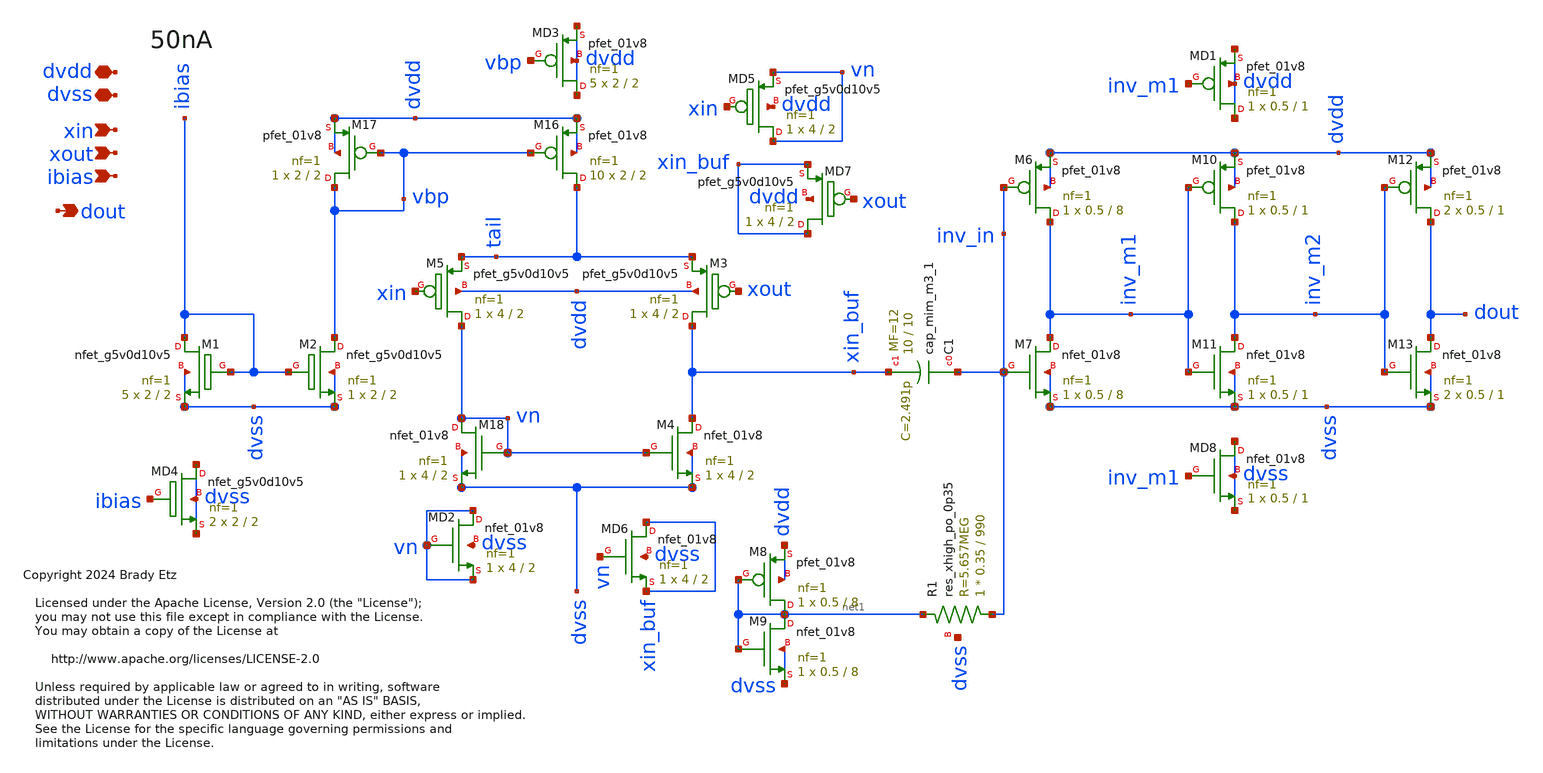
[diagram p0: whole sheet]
** sch_path: xschem/dout_amp.sch
* Copyright 2024 Brady Etz
* Licensed under the Apache License, Version 2.0 (the "License");
**.subckt dout_amp xin dvdd dvss dout ibias xout
*.ipin xin
*.iopin dvdd
*.iopin dvss
*.opin dout
*.ipin ibias
*.ipin xout
XM1 ibias ibias dvss dvss sky130_fd_pr__nfet_g5v0d10v5 L=2 W=2 nf=1 ad='int((nf+1)/2) * W/nf * 0.29'
+ as='int((nf+2)/2) * W/nf * 0.29' pd='2*int((nf+1)/2) * (W/nf + 0.29)' ps='2*int((nf+2)/2) * (W/nf + 0.29)'
+ nrd='0.29 / W' nrs='0.29 / W' sa=0 sb=0 sd=0 mult=5 m=5
XM2 vbp ibias dvss dvss sky130_fd_pr__nfet_g5v0d10v5 L=2 W=2 nf=1 ad='int((nf+1)/2) * W/nf * 0.29' as='int((nf+2)/2) * W/nf * 0.29'
+ pd='2*int((nf+1)/2) * (W/nf + 0.29)' ps='2*int((nf+2)/2) * (W/nf + 0.29)' nrd='0.29 / W' nrs='0.29 / W'
+ sa=0 sb=0 sd=0 mult=1 m=1
XM5 vn xin tail dvdd sky130_fd_pr__pfet_g5v0d10v5 L=2 W=4 nf=1 ad='int((nf+1)/2) * W/nf * 0.29' as='int((nf+2)/2) * W/nf * 0.29'
+ pd='2*int((nf+1)/2) * (W/nf + 0.29)' ps='2*int((nf+2)/2) * (W/nf + 0.29)' nrd='0.29 / W' nrs='0.29 / W'
+ sa=0 sb=0 sd=0 mult=1 m=1
XC1 inv_in xin_buf sky130_fd_pr__cap_mim_m3_1 W=10 L=10 MF=12 m=12
XM6 inv_m1 inv_in dvdd dvdd sky130_fd_pr__pfet_01v8 L=8 W=0.5 nf=1 ad='int((nf+1)/2) * W/nf * 0.29' as='int((nf+2)/2) * W/nf * 0.29'
+ pd='2*int((nf+1)/2) * (W/nf + 0.29)' ps='2*int((nf+2)/2) * (W/nf + 0.29)' nrd='0.29 / W' nrs='0.29 / W'
+ sa=0 sb=0 sd=0 mult=1 m=1
XM7 inv_m1 inv_in dvss dvss sky130_fd_pr__nfet_01v8 L=8 W=0.5 nf=1 ad='int((nf+1)/2) * W/nf * 0.29' as='int((nf+2)/2) * W/nf * 0.29'
+ pd='2*int((nf+1)/2) * (W/nf + 0.29)' ps='2*int((nf+2)/2) * (W/nf + 0.29)' nrd='0.29 / W' nrs='0.29 / W'
+ sa=0 sb=0 sd=0 mult=1 m=1
XM8 net1 net1 dvdd dvdd sky130_fd_pr__pfet_01v8 L=8 W=0.5 nf=1 ad='int((nf+1)/2) * W/nf * 0.29' as='int((nf+2)/2) * W/nf * 0.29'
+ pd='2*int((nf+1)/2) * (W/nf + 0.29)' ps='2*int((nf+2)/2) * (W/nf + 0.29)' nrd='0.29 / W' nrs='0.29 / W'
+ sa=0 sb=0 sd=0 mult=1 m=1
XM9 net1 net1 dvss dvss sky130_fd_pr__nfet_01v8 L=8 W=0.5 nf=1 ad='int((nf+1)/2) * W/nf * 0.29' as='int((nf+2)/2) * W/nf * 0.29'
+ pd='2*int((nf+1)/2) * (W/nf + 0.29)' ps='2*int((nf+2)/2) * (W/nf + 0.29)' nrd='0.29 / W' nrs='0.29 / W'
+ sa=0 sb=0 sd=0 mult=1 m=1
XR1 inv_in net1 dvss sky130_fd_pr__res_xhigh_po_0p35 L=990 mult=1 m=1
XM10 inv_m2 inv_m1 dvdd dvdd sky130_fd_pr__pfet_01v8 L=1 W=0.5 nf=1 ad='int((nf+1)/2) * W/nf * 0.29'
+ as='int((nf+2)/2) * W/nf * 0.29' pd='2*int((nf+1)/2) * (W/nf + 0.29)' ps='2*int((nf+2)/2) * (W/nf + 0.29)'
+ nrd='0.29 / W' nrs='0.29 / W' sa=0 sb=0 sd=0 mult=1 m=1
XM11 inv_m2 inv_m1 dvss dvss sky130_fd_pr__nfet_01v8 L=1 W=0.5 nf=1 ad='int((nf+1)/2) * W/nf * 0.29'
+ as='int((nf+2)/2) * W/nf * 0.29' pd='2*int((nf+1)/2) * (W/nf + 0.29)' ps='2*int((nf+2)/2) * (W/nf + 0.29)'
+ nrd='0.29 / W' nrs='0.29 / W' sa=0 sb=0 sd=0 mult=1 m=1
XM12 dout inv_m2 dvdd dvdd sky130_fd_pr__pfet_01v8 L=1 W=0.5 nf=1 ad='int((nf+1)/2) * W/nf * 0.29' as='int((nf+2)/2) * W/nf * 0.29'
+ pd='2*int((nf+1)/2) * (W/nf + 0.29)' ps='2*int((nf+2)/2) * (W/nf + 0.29)' nrd='0.29 / W' nrs='0.29 / W'
+ sa=0 sb=0 sd=0 mult=2 m=2
XM13 dout inv_m2 dvss dvss sky130_fd_pr__nfet_01v8 L=1 W=0.5 nf=1 ad='int((nf+1)/2) * W/nf * 0.29' as='int((nf+2)/2) * W/nf * 0.29'
+ pd='2*int((nf+1)/2) * (W/nf + 0.29)' ps='2*int((nf+2)/2) * (W/nf + 0.29)' nrd='0.29 / W' nrs='0.29 / W'
+ sa=0 sb=0 sd=0 mult=2 m=2
XM16 tail vbp dvdd dvdd sky130_fd_pr__pfet_01v8 L=2 W=2 nf=1 ad='int((nf+1)/2) * W/nf * 0.29' as='int((nf+2)/2) * W/nf * 0.29'
+ pd='2*int((nf+1)/2) * (W/nf + 0.29)' ps='2*int((nf+2)/2) * (W/nf + 0.29)' nrd='0.29 / W' nrs='0.29 / W'
+ sa=0 sb=0 sd=0 mult=10 m=10
XM17 vbp vbp dvdd dvdd sky130_fd_pr__pfet_01v8 L=2 W=2 nf=1 ad='int((nf+1)/2) * W/nf * 0.29' as='int((nf+2)/2) * W/nf * 0.29'
+ pd='2*int((nf+1)/2) * (W/nf + 0.29)' ps='2*int((nf+2)/2) * (W/nf + 0.29)' nrd='0.29 / W' nrs='0.29 / W'
+ sa=0 sb=0 sd=0 mult=1 m=1
XM3 xin_buf xout tail dvdd sky130_fd_pr__pfet_g5v0d10v5 L=2 W=4 nf=1 ad='int((nf+1)/2) * W/nf * 0.29'
+ as='int((nf+2)/2) * W/nf * 0.29' pd='2*int((nf+1)/2) * (W/nf + 0.29)' ps='2*int((nf+2)/2) * (W/nf + 0.29)'
+ nrd='0.29 / W' nrs='0.29 / W' sa=0 sb=0 sd=0 mult=1 m=1
XM4 xin_buf vn dvss dvss sky130_fd_pr__nfet_01v8 L=2 W=4 nf=1 ad='int((nf+1)/2) * W/nf * 0.29' as='int((nf+2)/2) * W/nf * 0.29'
+ pd='2*int((nf+1)/2) * (W/nf + 0.29)' ps='2*int((nf+2)/2) * (W/nf + 0.29)' nrd='0.29 / W' nrs='0.29 / W'
+ sa=0 sb=0 sd=0 mult=1 m=1
XM18 vn vn dvss dvss sky130_fd_pr__nfet_01v8 L=2 W=4 nf=1 ad='int((nf+1)/2) * W/nf * 0.29' as='int((nf+2)/2) * W/nf * 0.29'
+ pd='2*int((nf+1)/2) * (W/nf + 0.29)' ps='2*int((nf+2)/2) * (W/nf + 0.29)' nrd='0.29 / W' nrs='0.29 / W'
+ sa=0 sb=0 sd=0 mult=1 m=1
XMD2 vn vn vn dvss sky130_fd_pr__nfet_01v8 L=2 W=4 nf=1 ad='int((nf+1)/2) * W/nf * 0.29' as='int((nf+2)/2) * W/nf * 0.29'
+ pd='2*int((nf+1)/2) * (W/nf + 0.29)' ps='2*int((nf+2)/2) * (W/nf + 0.29)' nrd='0.29 / W' nrs='0.29 / W'
+ sa=0 sb=0 sd=0 mult=1 m=1
XMD1 dvdd inv_m1 dvdd dvdd sky130_fd_pr__pfet_01v8 L=1 W=0.5 nf=1 ad='int((nf+1)/2) * W/nf * 0.29' as='int((nf+2)/2) * W/nf * 0.29'
+ pd='2*int((nf+1)/2) * (W/nf + 0.29)' ps='2*int((nf+2)/2) * (W/nf + 0.29)' nrd='0.29 / W' nrs='0.29 / W'
+ sa=0 sb=0 sd=0 mult=1 m=1
XMD4 dvss ibias dvss dvss sky130_fd_pr__nfet_g5v0d10v5 L=2 W=2 nf=1 ad='int((nf+1)/2) * W/nf * 0.29'
+ as='int((nf+2)/2) * W/nf * 0.29' pd='2*int((nf+1)/2) * (W/nf + 0.29)' ps='2*int((nf+2)/2) * (W/nf + 0.29)'
+ nrd='0.29 / W' nrs='0.29 / W' sa=0 sb=0 sd=0 mult=2 m=2
XMD3 dvdd vbp dvdd dvdd sky130_fd_pr__pfet_01v8 L=2 W=2 nf=1 ad='int((nf+1)/2) * W/nf * 0.29' as='int((nf+2)/2) * W/nf * 0.29'
+ pd='2*int((nf+1)/2) * (W/nf + 0.29)' ps='2*int((nf+2)/2) * (W/nf + 0.29)' nrd='0.29 / W' nrs='0.29 / W'
+ sa=0 sb=0 sd=0 mult=5 m=5
XMD5 vn xin vn dvdd sky130_fd_pr__pfet_g5v0d10v5 L=2 W=4 nf=1 ad='int((nf+1)/2) * W/nf * 0.29' as='int((nf+2)/2) * W/nf * 0.29'
+ pd='2*int((nf+1)/2) * (W/nf + 0.29)' ps='2*int((nf+2)/2) * (W/nf + 0.29)' nrd='0.29 / W' nrs='0.29 / W'
+ sa=0 sb=0 sd=0 mult=1 m=1
XMD6 xin_buf vn xin_buf dvss sky130_fd_pr__nfet_01v8 L=2 W=4 nf=1 ad='int((nf+1)/2) * W/nf * 0.29' as='int((nf+2)/2) * W/nf * 0.29'
+ pd='2*int((nf+1)/2) * (W/nf + 0.29)' ps='2*int((nf+2)/2) * (W/nf + 0.29)' nrd='0.29 / W' nrs='0.29 / W'
+ sa=0 sb=0 sd=0 mult=1 m=1
XMD7 xin_buf xout xin_buf dvdd sky130_fd_pr__pfet_g5v0d10v5 L=2 W=4 nf=1 ad='int((nf+1)/2) * W/nf * 0.29'
+ as='int((nf+2)/2) * W/nf * 0.29' pd='2*int((nf+1)/2) * (W/nf + 0.29)' ps='2*int((nf+2)/2) * (W/nf + 0.29)'
+ nrd='0.29 / W' nrs='0.29 / W' sa=0 sb=0 sd=0 mult=1 m=1
XMD8 dvss inv_m1 dvss dvss sky130_fd_pr__nfet_01v8 L=1 W=0.5 nf=1 ad='int((nf+1)/2) * W/nf * 0.29' as='int((nf+2)/2) * W/nf * 0.29'
+ pd='2*int((nf+1)/2) * (W/nf + 0.29)' ps='2*int((nf+2)/2) * (W/nf + 0.29)' nrd='0.29 / W' nrs='0.29 / W'
+ sa=0 sb=0 sd=0 mult=1 m=1
**.ends
.end
